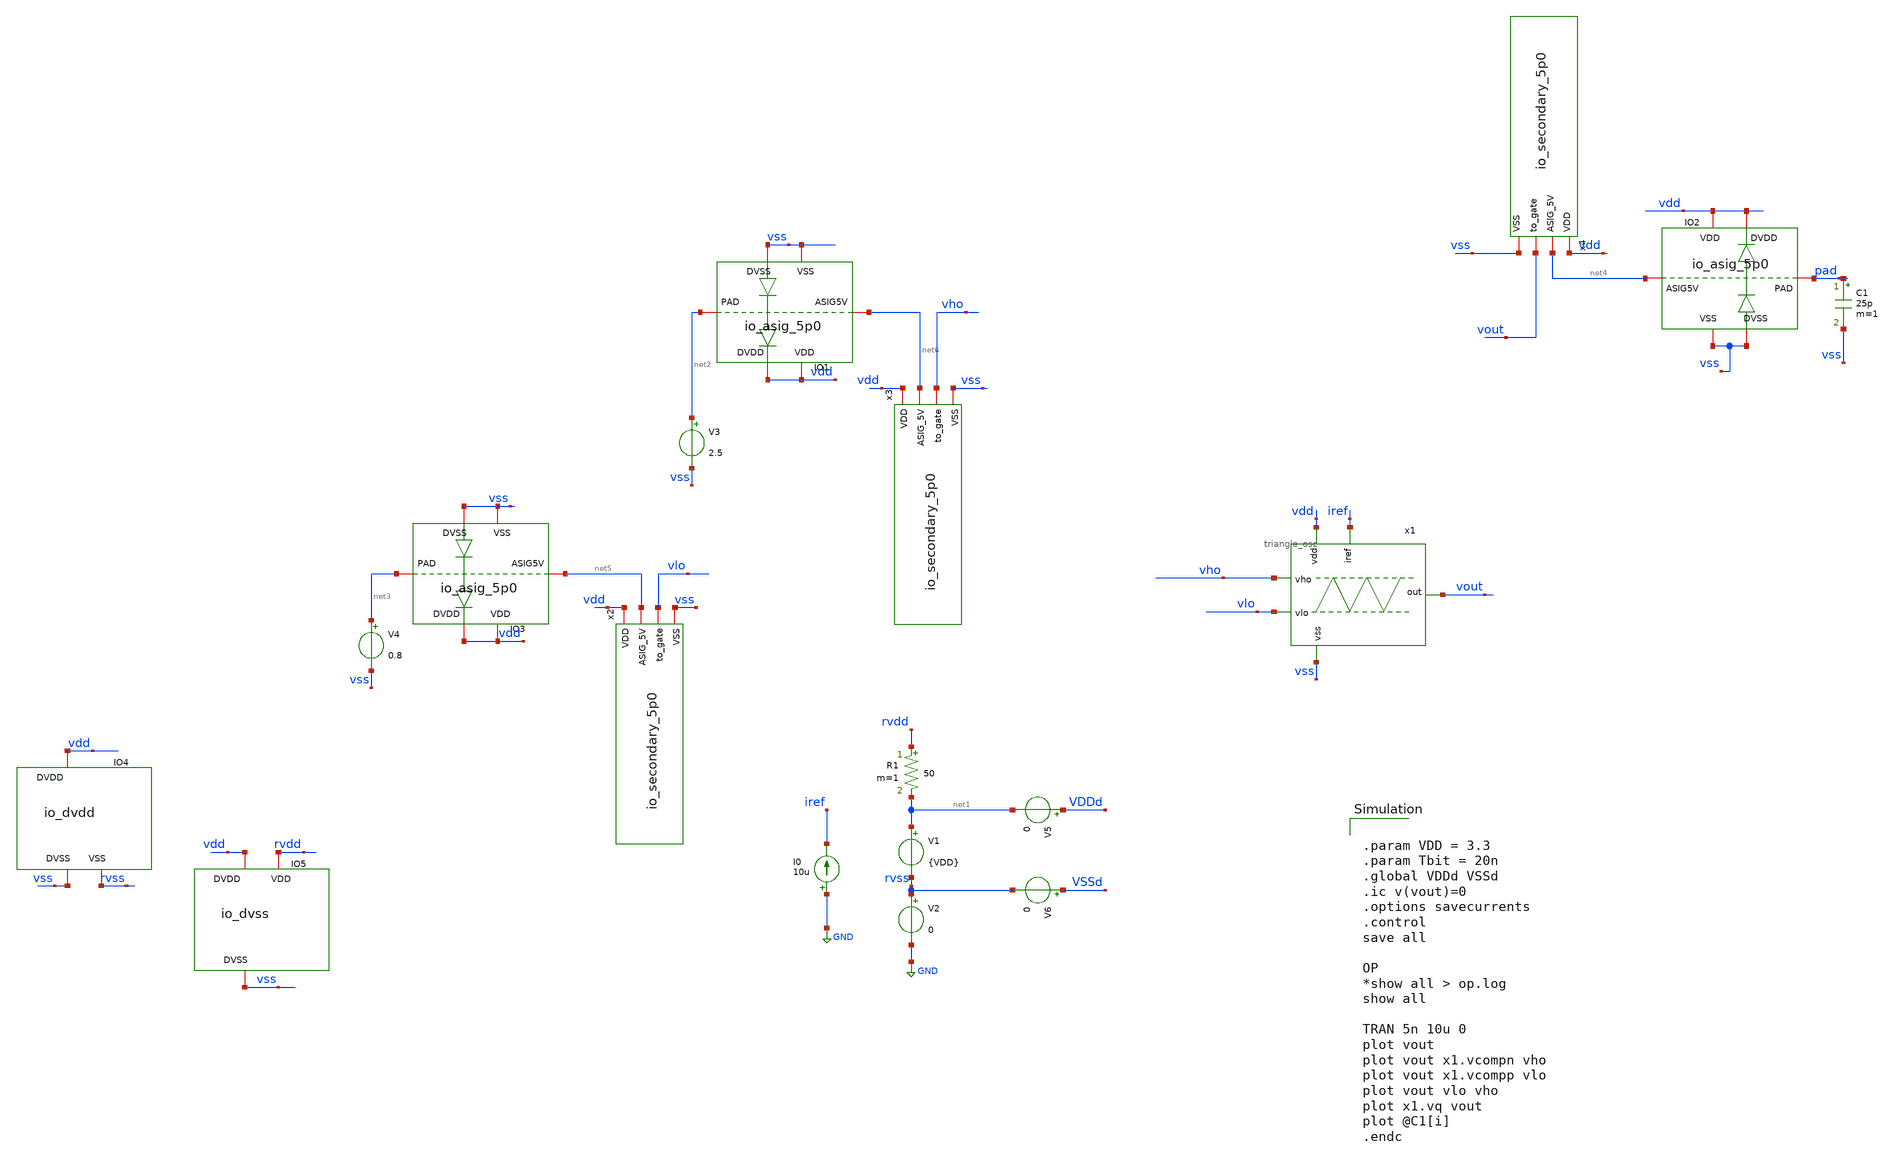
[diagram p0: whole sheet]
** sch_path: designs/libs/tb_analog_pads_pex/oscillator/test_oscillator.sch
**.subckt test_oscillator
x1 vdd vho vout vlo iref vss triangle_osc
V1 net1 rvss {VDD}
V2 rvss GND 0
V3 net2 vss 2.5
V4 net3 vss 0.8
I0 GND iref 10u
C1 pad vss 25p m=1
V5 VDDd net1 0
V6 VSSd rvss 0
R1 rvdd net1 50 m=1
XIO2 vss vdd vss vdd pad net4 gf180mcu_fd_io__asig_5p0_extracted
XIO1 vss vdd vss vdd net2 net6 gf180mcu_fd_io__asig_5p0_extracted
XIO3 vss vdd vss vdd net3 net5 gf180mcu_fd_io__asig_5p0_extracted
x2 vdd net5 vlo vss io_secondary_5p0
x3 vdd net6 vho vss io_secondary_5p0
x4 vdd net4 vout vss io_secondary_5p0
XIO4 vdd vss rvss gf180mcu_fd_io__dvdd
XIO5 vdd vss rvdd gf180mcu_fd_io__dvss
**** begin user architecture code


.param VDD = 3.3
.param Tbit = 20n
.global VDDd VSSd
.ic v(vout)=0
.options savecurrents
.control
save all

OP
*show all > op.log
show all

TRAN 5n 10u 0
plot vout
plot vout x1.vcompn vho
plot vout x1.vcompp vlo
plot vout vlo vho
plot x1.vq vout
plot @C1[i]
.endc



.include /foss/designs/libs/core_analog/Chipathon2025_pads/xschem/gf180mcu_fd_io.spice
.include /foss/designs/libs/core_analog/Chipathon2025_pads/xschem/gf180mcu_fd_io__asig_5p0_extracted.spice
.include $::180MCU_MODELS/design.ngspice
.include /foss/pdks/gf180mcuD/libs.ref/gf180mcu_fd_sc_mcu9t5v0/spice/gf180mcu_fd_sc_mcu9t5v0.spice
.lib $::180MCU_MODELS/sm141064.ngspice typical
.lib $::180MCU_MODELS/sm141064.ngspice cap_mim
.lib $::180MCU_MODELS/sm141064.ngspice mimcap_typical
.lib $::180MCU_MODELS/sm141064.ngspice diode_typical
.lib $::180MCU_MODELS/sm141064.ngspice res_typical
.lib $::180MCU_MODELS/sm141064.ngspice moscap_typical

**** end user architecture code
**.ends

* expanding   symbol:  libs/core_analog/oscillator/triangle_osc.sym # of pins=6
** sym_path: libs/core_analog/oscillator/triangle_osc.sym
** sch_path: libs/core_analog/oscillator/triangle_osc.sch
.subckt triangle_osc vdd vho out vlo iref vss
*.ipin iref
*.ipin vss
*.ipin vho
*.ipin vlo
*.opin out
*.ipin vdd
XM1 net1 iref vss vss nfet_03v3 L=1u W=2.5u nf=1 ad='int((nf+1)/2) * W/nf * 0.18u' as='int((nf+2)/2) * W/nf * 0.18u'
+ pd='2*int((nf+1)/2) * (W/nf + 0.18u)' ps='2*int((nf+2)/2) * (W/nf + 0.18u)' nrd='0.18u / W' nrs='0.18u / W'
+ sa=0 sb=0 sd=0 m=3
XM8 net2 iref vss vss nfet_03v3 L=1u W=2.5u nf=1 ad='int((nf+1)/2) * W/nf * 0.18u' as='int((nf+2)/2) * W/nf * 0.18u'
+ pd='2*int((nf+1)/2) * (W/nf + 0.18u)' ps='2*int((nf+2)/2) * (W/nf + 0.18u)' nrd='0.18u / W' nrs='0.18u / W'
+ sa=0 sb=0 sd=0 m=3
XM4 net1 net1 vdd vdd pfet_03v3 L=1u W=4.5u nf=1 ad='int((nf+1)/2) * W/nf * 0.18u' as='int((nf+2)/2) * W/nf * 0.18u'
+ pd='2*int((nf+1)/2) * (W/nf + 0.18u)' ps='2*int((nf+2)/2) * (W/nf + 0.18u)' nrd='0.18u / W' nrs='0.18u / W'
+ sa=0 sb=0 sd=0 m=3
XM5 net3 net1 vdd vdd pfet_03v3 L=1u W=4.5u nf=1 ad='int((nf+1)/2) * W/nf * 0.18u' as='int((nf+2)/2) * W/nf * 0.18u'
+ pd='2*int((nf+1)/2) * (W/nf + 0.18u)' ps='2*int((nf+2)/2) * (W/nf + 0.18u)' nrd='0.18u / W' nrs='0.18u / W'
+ sa=0 sb=0 sd=0 m=3
XM6 out nq net3 vdd pfet_03v3 L=0.3u W=4u nf=1 ad='int((nf+1)/2) * W/nf * 0.18u' as='int((nf+2)/2) * W/nf * 0.18u'
+ pd='2*int((nf+1)/2) * (W/nf + 0.18u)' ps='2*int((nf+2)/2) * (W/nf + 0.18u)' nrd='0.18u / W' nrs='0.18u / W'
+ sa=0 sb=0 sd=0 m=2
XM7 out nq net2 vss nfet_03v3 L=0.3u W=4u nf=1 ad='int((nf+1)/2) * W/nf * 0.18u' as='int((nf+2)/2) * W/nf * 0.18u'
+ pd='2*int((nf+1)/2) * (W/nf + 0.18u)' ps='2*int((nf+2)/2) * (W/nf + 0.18u)' nrd='0.18u / W' nrs='0.18u / W'
+ sa=0 sb=0 sd=0 m=1
XM2 iref iref vss vss nfet_03v3 L=1u W=2.5u nf=1 ad='int((nf+1)/2) * W/nf * 0.18u' as='int((nf+2)/2) * W/nf * 0.18u'
+ pd='2*int((nf+1)/2) * (W/nf + 0.18u)' ps='2*int((nf+2)/2) * (W/nf + 0.18u)' nrd='0.18u / W' nrs='0.18u / W'
+ sa=0 sb=0 sd=0 m=1
XM10 net5 iref vss vss nfet_03v3 L=1u W=2.5u nf=1 ad='int((nf+1)/2) * W/nf * 0.18u' as='int((nf+2)/2) * W/nf * 0.18u'
+ pd='2*int((nf+1)/2) * (W/nf + 0.18u)' ps='2*int((nf+2)/2) * (W/nf + 0.18u)' nrd='0.18u / W' nrs='0.18u / W'
+ sa=0 sb=0 sd=0 m=1
XM9 net4 net1 vdd vdd pfet_03v3 L=1u W=4.5u nf=1 ad='int((nf+1)/2) * W/nf * 0.18u' as='int((nf+2)/2) * W/nf * 0.18u'
+ pd='2*int((nf+1)/2) * (W/nf + 0.18u)' ps='2*int((nf+2)/2) * (W/nf + 0.18u)' nrd='0.18u / W' nrs='0.18u / W'
+ sa=0 sb=0 sd=0 m=1
**** begin user architecture code

.include $::180MCU_MODELS/design.ngspice
.include /foss/pdks/gf180mcuD/libs.ref/gf180mcu_fd_sc_mcu9t5v0/spice/gf180mcu_fd_sc_mcu9t5v0.spice
.lib $::180MCU_MODELS/sm141064.ngspice typical

**** end user architecture code
xn_comp vdd vcompn vho vss out net4 Nmos_Comparator
xp_comp vdd vcompp out vss vlo net5 Pmos_Comparator
x1 vcompp q nq vcompn sr_latch
.ends


* expanding   symbol:  libs/core_analog/ESD/io_secondary_5p0.sym # of pins=4
** sym_path: designs/libs/core_analog/ESD/io_secondary_5p0.sym
** sch_path: designs/libs/core_analog/ESD/io_secondary_5p0.sch
.subckt io_secondary_5p0 VDD ASIG_5V to_gate VSS
*.iopin VSS
*.iopin VDD
*.iopin to_gate
*.iopin ASIG_5V
D1 VSS to_gate diode_nd2ps_06v0 area='10u * 10u ' pj='2*10u + 2*10u ' m=1
D2 to_gate VDD diode_pd2nw_03v3 area='10u * 10u ' pj='2*10u + 2*10u ' m=1
XR1 to_gate ASIG_5V VDD ppolyf_u r_width=16e-6 r_length=4e-6 m=1
.ends


* expanding   symbol:  libs/core_analog/Comparator/Nmos_Comparator.sym # of pins=6
** sym_path: designs/libs/core_analog/Comparator/Nmos_Comparator.sym
** sch_path: designs/libs/core_analog/Comparator/Nmos_Comparator.sch
.subckt Nmos_Comparator vdd vout inp vss inn iref
*.ipin vss
*.ipin vdd
*.ipin iref
*.ipin inn
*.ipin inp
*.opin vout
XM3 net1 net1 vss vss nfet_03v3 L=1u W=3.5u nf=1 ad='int((nf+1)/2) * W/nf * 0.18u' as='int((nf+2)/2) * W/nf * 0.18u'
+ pd='2*int((nf+1)/2) * (W/nf + 0.18u)' ps='2*int((nf+2)/2) * (W/nf + 0.18u)' nrd='0.18u / W' nrs='0.18u / W'
+ sa=0 sb=0 sd=0 m=1
XM4 vout net1 vss vss nfet_03v3 L=1u W=3.5u nf=1 ad='int((nf+1)/2) * W/nf * 0.18u' as='int((nf+2)/2) * W/nf * 0.18u'
+ pd='2*int((nf+1)/2) * (W/nf + 0.18u)' ps='2*int((nf+2)/2) * (W/nf + 0.18u)' nrd='0.18u / W' nrs='0.18u / W'
+ sa=0 sb=0 sd=0 m=1
XM5 net2 inn net3 vss nfet_03v3 L=1u W=4u nf=1 ad='int((nf+1)/2) * W/nf * 0.18u' as='int((nf+2)/2) * W/nf * 0.18u'
+ pd='2*int((nf+1)/2) * (W/nf + 0.18u)' ps='2*int((nf+2)/2) * (W/nf + 0.18u)' nrd='0.18u / W' nrs='0.18u / W'
+ sa=0 sb=0 sd=0 m=1
XM6 net4 inp net3 vss nfet_03v3 L=1u W=4u nf=1 ad='int((nf+1)/2) * W/nf * 0.18u' as='int((nf+2)/2) * W/nf * 0.18u'
+ pd='2*int((nf+1)/2) * (W/nf + 0.18u)' ps='2*int((nf+2)/2) * (W/nf + 0.18u)' nrd='0.18u / W' nrs='0.18u / W'
+ sa=0 sb=0 sd=0 m=1
XM7 net1 net2 vdd vdd pfet_03v3 L=0.5u W=16.5u nf=4 ad='int((nf+1)/2) * W/nf * 0.18u' as='int((nf+2)/2) * W/nf * 0.18u'
+ pd='2*int((nf+1)/2) * (W/nf + 0.18u)' ps='2*int((nf+2)/2) * (W/nf + 0.18u)' nrd='0.18u / W' nrs='0.18u / W'
+ sa=0 sb=0 sd=0 m=1
XM9 net4 net4 vdd vdd pfet_03v3 L=0.5u W=10u nf=2 ad='int((nf+1)/2) * W/nf * 0.18u' as='int((nf+2)/2) * W/nf * 0.18u'
+ pd='2*int((nf+1)/2) * (W/nf + 0.18u)' ps='2*int((nf+2)/2) * (W/nf + 0.18u)' nrd='0.18u / W' nrs='0.18u / W'
+ sa=0 sb=0 sd=0 m=1
XM11 net2 net2 vdd vdd pfet_03v3 L=0.5u W=10u nf=2 ad='int((nf+1)/2) * W/nf * 0.18u' as='int((nf+2)/2) * W/nf * 0.18u'
+ pd='2*int((nf+1)/2) * (W/nf + 0.18u)' ps='2*int((nf+2)/2) * (W/nf + 0.18u)' nrd='0.18u / W' nrs='0.18u / W'
+ sa=0 sb=0 sd=0 m=1
XM12 vout net4 vdd vdd pfet_03v3 L=0.5u W=16.5u nf=4 ad='int((nf+1)/2) * W/nf * 0.18u' as='int((nf+2)/2) * W/nf * 0.18u'
+ pd='2*int((nf+1)/2) * (W/nf + 0.18u)' ps='2*int((nf+2)/2) * (W/nf + 0.18u)' nrd='0.18u / W' nrs='0.18u / W'
+ sa=0 sb=0 sd=0 m=1
XM1 net4 net2 vdd vdd pfet_03v3 L=0.5u W=10u nf=2 ad='int((nf+1)/2) * W/nf * 0.18u' as='int((nf+2)/2) * W/nf * 0.18u'
+ pd='2*int((nf+1)/2) * (W/nf + 0.18u)' ps='2*int((nf+2)/2) * (W/nf + 0.18u)' nrd='0.18u / W' nrs='0.18u / W'
+ sa=0 sb=0 sd=0 m=1
XM2 net2 net4 vdd vdd pfet_03v3 L=0.5u W=10u nf=2 ad='int((nf+1)/2) * W/nf * 0.18u' as='int((nf+2)/2) * W/nf * 0.18u'
+ pd='2*int((nf+1)/2) * (W/nf + 0.18u)' ps='2*int((nf+2)/2) * (W/nf + 0.18u)' nrd='0.18u / W' nrs='0.18u / W'
+ sa=0 sb=0 sd=0 m=1
XM8 iref iref vss vss nfet_03v3 L=1u W=2.5u nf=1 ad='int((nf+1)/2) * W/nf * 0.18u' as='int((nf+2)/2) * W/nf * 0.18u'
+ pd='2*int((nf+1)/2) * (W/nf + 0.18u)' ps='2*int((nf+2)/2) * (W/nf + 0.18u)' nrd='0.18u / W' nrs='0.18u / W'
+ sa=0 sb=0 sd=0 m=1
XM10 net3 iref vss vss nfet_03v3 L=1u W=5u nf=2 ad='int((nf+1)/2) * W/nf * 0.18u' as='int((nf+2)/2) * W/nf * 0.18u'
+ pd='2*int((nf+1)/2) * (W/nf + 0.18u)' ps='2*int((nf+2)/2) * (W/nf + 0.18u)' nrd='0.18u / W' nrs='0.18u / W'
+ sa=0 sb=0 sd=0 m=1
.ends


* expanding   symbol:  libs/core_analog/oscillator/sr_latch.sym # of pins=4
** sym_path: designs/libs/core_analog/oscillator/sr_latch.sym
** sch_path: designs/libs/core_analog/oscillator/sr_latch.sch
.subckt sr_latch R Q NOTQ S
*.ipin R
*.ipin S
*.opin Q
*.opin NOTQ
x1 R NOTQ VSSd VDDd VSSd VDDd Q gf180mcu_fd_sc_mcu9t5v0__nor2_2
x2 Q S VSSd VDDd VSSd VDDd NOTQ gf180mcu_fd_sc_mcu9t5v0__nor2_2
**** begin user architecture code

.include $::180MCU_MODELS/design.ngspice
.include /foss/pdks/gf180mcuD/libs.ref/gf180mcu_fd_sc_mcu9t5v0/spice/gf180mcu_fd_sc_mcu9t5v0.spice
.lib $::180MCU_MODELS/sm141064.ngspice typical

**** end user architecture code
.ends

.GLOBAL GND
.end
